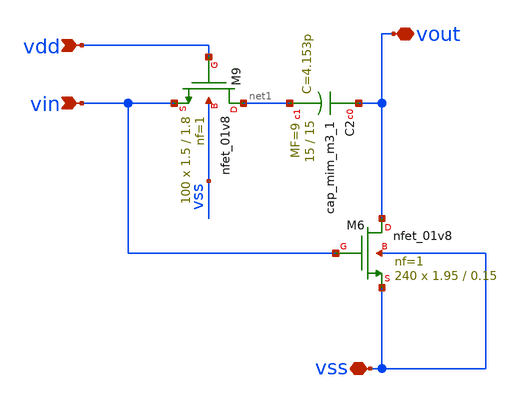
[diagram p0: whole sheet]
** sch_path: track_analogico/opamp_ramiro/output.sch
**.subckt output vss vin vout vdd
*.iopin vss
*.ipin vin
*.iopin vout
*.ipin vdd
XM6 vout vin vss vss sky130_fd_pr__nfet_01v8 L=0.15 W=1.95 nf=1 ad='W * 0.29' as='W * 0.29' pd='2 * (W + 0.29)'
+ ps='2 * (W + 0.29)' nrd='0.29 / W' nrs='0.29 / W' sa=0 sb=0 sd=0 mult=240 m=240
XM9 net1 vdd vin vss sky130_fd_pr__nfet_01v8 L=1.8 W=1.5 nf=1 ad='W * 0.29' as='W * 0.29' pd='2 * (W + 0.29)'
+ ps='2 * (W + 0.29)' nrd='0.29 / W' nrs='0.29 / W' sa=0 sb=0 sd=0 mult=100 m=100
XC2 vout net1 sky130_fd_pr__cap_mim_m3_1 W=15 L=15 MF=9 m=9
**.ends
.end
